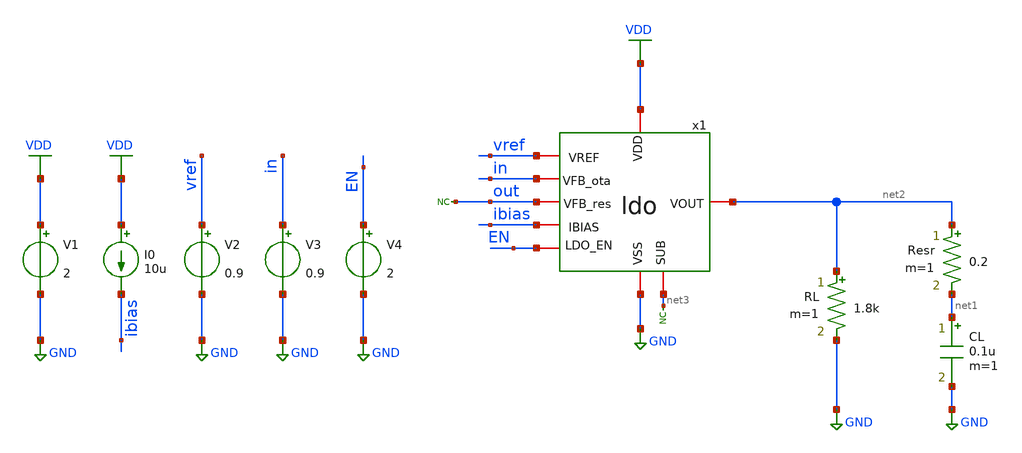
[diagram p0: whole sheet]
** sch_path: designs/libs/tb_ldo/tb_ldo_ac/tb_ldo_ac.sch
**.subckt tb_ldo_ac
RL net2 GND 1.8k m=1
V1 VDD GND 2
V2 vref GND 0.9
I0 VDD ibias 10u
CL net1 GND 0.1u m=1
Resr net2 net1 0.2 m=1
V3 in GND 0.9
* noconn out
* noconn #net3
x1 VDD vref net2 ibias net3 GND EN in out ldo
V4 EN GND 2
**** begin user architecture code



.control
save all

run
set color0 = white

** Set sources
alter @V3[AC] = 1

** Simulations
ac dec 100 1 10G

** Plots
setplot ac1
let gain_db = db(v(out))
let gain_db_ota = db(v(x1.vota))
plot gain_db
plot gain_db_ota

** Measurements
meas ac DC_gain FIND gain_db AT=1Hz
let gain_3db = DC_gain-3
meas ac f_3db WHEN gain_db = $&gain_3db
meas ac f_0db WHEN gain_db = 0

write tb_ldo_ac.raw
.endc
* ngspice commands




.include $::180MCU_MODELS/design.ngspice
.lib $::180MCU_MODELS/sm141064.ngspice typical
.lib $::180MCU_MODELS/sm141064.ngspice cap_mim
.lib $::180MCU_MODELS/sm141064.ngspice moscap_typical
.lib $::180MCU_MODELS/sm141064.ngspice mimcap_typical
.lib $::180MCU_MODELS/sm141064.ngspice res_typical
* .lib $::180MCU_MODELS/sm141064.ngspice res_statistical
* ngspice commands

**** end user architecture code
**.ends
.GLOBAL GND
.GLOBAL VDD
.end
